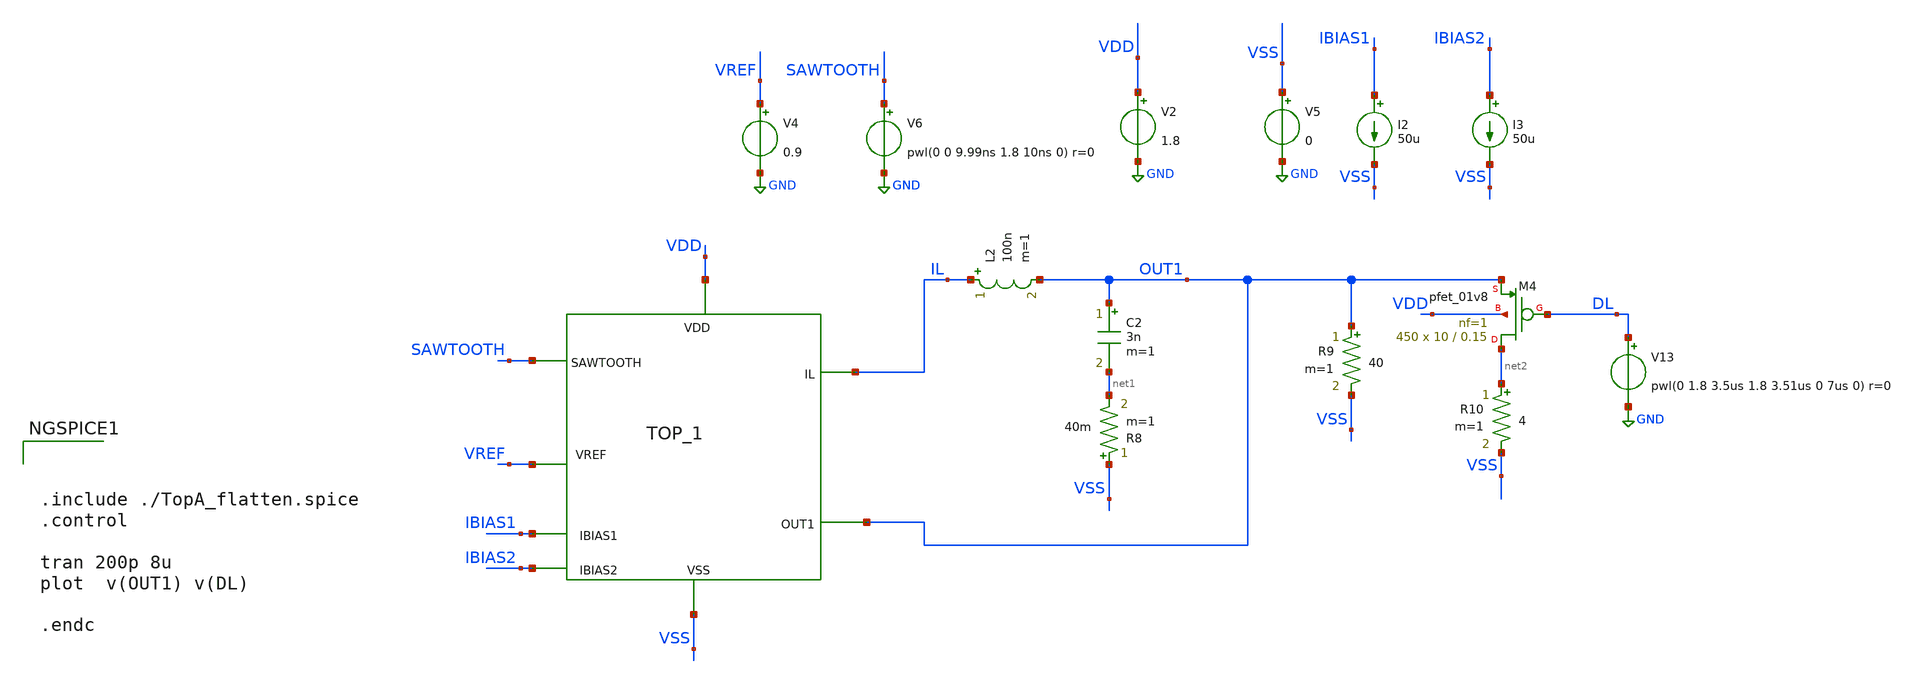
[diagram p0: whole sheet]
** sch_path: xschem/DC_DC_Converter_xschem/DC_DC_Converter/TOP_LEVEL/Top_Final/PEX_TOP/Top_1_PEX_TB.sch
**.subckt Top_1_PEX_TB
V2 VDD GND 1.8
V5 VSS GND 0
V4 VREF GND 0.9
V6 SAWTOOTH GND pwl(0 0 9.99ns 1.8 10ns 0) r=0
I2 IBIAS1 VSS 50u
I3 IBIAS2 VSS 50u
L2 IL OUT1 100n m=1
C2 OUT1 net1 3n m=1
R8 VSS net1 40m m=1
XM4 net2 DL OUT1 VDD sky130_fd_pr__pfet_01v8 L=0.15 W=10 nf=1 ad='int((nf+1)/2) * W/nf * 0.29' as='int((nf+2)/2) * W/nf * 0.29'
+ pd='2*int((nf+1)/2) * (W/nf + 0.29)' ps='2*int((nf+2)/2) * (W/nf + 0.29)' nrd='0.29 / W' nrs='0.29 / W'
+ sa=0 sb=0 sd=0 mult=450 m=450
V13 DL GND pwl(0 1.8 3.5us 1.8 3.51us 0 7us 0) r=0
R9 OUT1 VSS 40 m=1
R10 net2 VSS 4 m=1
XTOPA1 VDD VSS SAWTOOTH VREF IBIAS1 OUT1 IBIAS2 IL Top_1_PEX
**** begin user architecture code
** manual skywater pdks install (with patches applied)
* .lib $::SKYWATER_MODELS/models/sky130.lib.spice tt

** opencircuitdesign pdks install
.lib $::SKYWATER_MODELS/sky130.lib.spice tt
.include $::SKYWATER_STDCELLS/sky130_fd_sc_hd.spice




.include ./TopA_flatten.spice
.control

tran 200p 8u
plot  v(OUT1) v(DL)

.endc


**** end user architecture code
**.ends
.GLOBAL GND
.end
